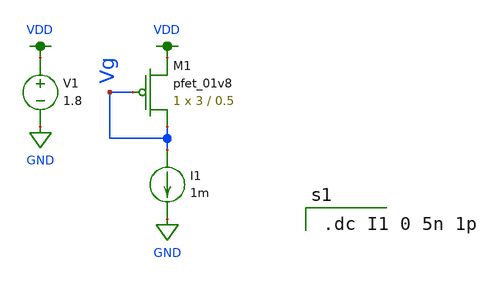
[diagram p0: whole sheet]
** sch_path: mp3/xschem/test_pmos.sch
**.subckt test_pmos
XM1 Vg Vg VDD VDD sky130_fd_pr__pfet_01v8 L=0.5 W=3 nf=1 ad='int((nf+1)/2) * W/nf * 0.29' as='int((nf+2)/2) * W/nf * 0.29'
+ pd='2*int((nf+1)/2) * (W/nf + 0.29)' ps='2*int((nf+2)/2) * (W/nf + 0.29)' nrd='0.29 / W' nrs='0.29 / W'
+ sa=0 sb=0 sd=0 mult=1 m=1
V1 VDD GND 1.8
I1 Vg GND 1m
**** begin user architecture code

.option wnflag=1
.lib ~/skywater/skywater-pdk/libraries/sky130_fd_pr_ngspice/latest/models/sky130.lib.spice tt


.dc I1 0 5n 1p

**** end user architecture code
**.ends
.GLOBAL VDD
.GLOBAL GND
.end
